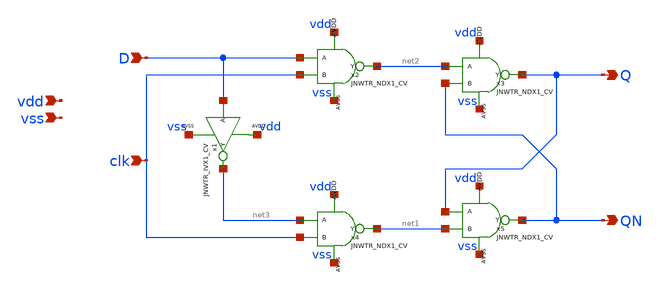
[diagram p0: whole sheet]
** sch_path: design/JNW_AVV_SKY130A/DFF.sch
**.subckt DFF vdd vss clk Q D QN
*.ipin vdd
*.ipin vss
*.ipin clk
*.opin Q
*.ipin D
*.opin QN
x1 D net3 vdd vss JNWTR_IVX1_CV
x2 D clk net2 vdd vss JNWTR_NDX1_CV
x3 net2 QN Q vdd vss JNWTR_NDX1_CV
x4 net3 clk net1 vdd vss JNWTR_NDX1_CV
x5 Q net1 QN vdd vss JNWTR_NDX1_CV
**.ends
.end
